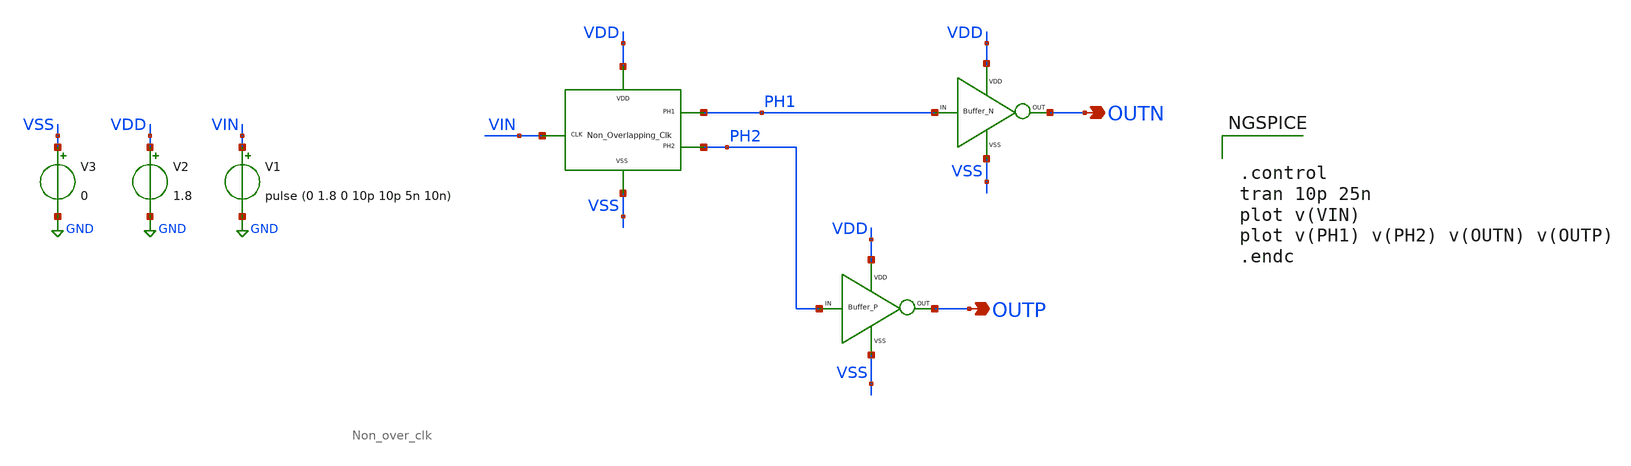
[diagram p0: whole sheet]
** sch_path: xschem/DC_DC_Converter_xschem/OTHERS/DC_DC_Converter_V7/Non_Overlap_Clk/Non_over_clk_V3_test.sch
**.subckt Non_over_clk_V3_test OUTP OUTN
*.opin OUTP
*.opin OUTN
V1 VIN GND pulse (0 1.8 0 10p 10p 5n 10n)
V2 VDD GND 1.8
V3 VSS GND 0
x1 VDD VIN PH1 VSS PH2 Non_over_clk
X3 PH1 OUTN VDD VSS BUFFER_N
X2 PH2 OUTP VDD VSS BUFFER_P
**** begin user architecture code


.control
tran 10p 25n
plot v(VIN)
plot v(PH1) v(PH2) v(OUTN) v(OUTP)
.endc

** manual skywater pdks install (with patches applied)
* .lib $::SKYWATER_MODELS/models/sky130.lib.spice tt

** opencircuitdesign pdks install
.lib $::SKYWATER_MODELS/sky130.lib.spice tt
.include $::SKYWATER_STDCELLS/sky130_fd_sc_hd.spice

**** end user architecture code
**.ends
.GLOBAL GND
.end
